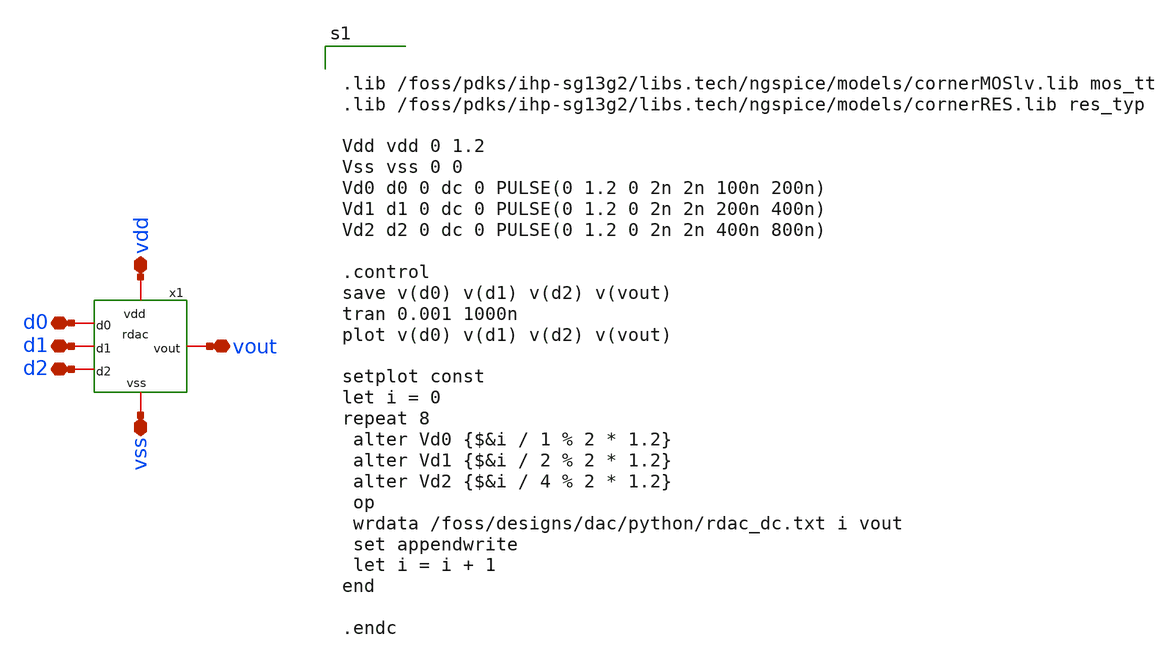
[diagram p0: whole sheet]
** sch_path: xschem/rdac_tb.sch
**.subckt rdac_tb vout vss d0 d1 d2 vdd
*.iopin vout
*.iopin vss
*.iopin d0
*.iopin d1
*.iopin d2
*.iopin vdd
x1 vdd d0 vout d1 d2 vss rdac
**** begin user architecture code


.lib /foss/pdks/ihp-sg13g2/libs.tech/ngspice/models/cornerMOSlv.lib mos_tt
.lib /foss/pdks/ihp-sg13g2/libs.tech/ngspice/models/cornerRES.lib res_typ

Vdd vdd 0 1.2
Vss vss 0 0
Vd0 d0 0 dc 0 PULSE(0 1.2 0 2n 2n 100n 200n)
Vd1 d1 0 dc 0 PULSE(0 1.2 0 2n 2n 200n 400n)
Vd2 d2 0 dc 0 PULSE(0 1.2 0 2n 2n 400n 800n)

.control
save v(d0) v(d1) v(d2) v(vout)
tran 0.001 1000n
plot v(d0) v(d1) v(d2) v(vout)

setplot const
let i = 0
repeat 8
 alter Vd0 {$&i / 1 % 2 * 1.2}
 alter Vd1 {$&i / 2 % 2 * 1.2}
 alter Vd2 {$&i / 4 % 2 * 1.2}
 op
 wrdata /foss/designs/dac/python/rdac_dc.txt i vout
 set appendwrite
 let i = i + 1
end

.endc


**** end user architecture code
**.ends

* expanding   symbol:  rdac.sym # of pins=6
** sym_path: xschem/rdac.sym
** sch_path: xschem/rdac.sch
.subckt rdac vdd d0 vout d1 d2 vss
*.iopin vout
*.iopin vdd
*.iopin d0
*.iopin vss
*.iopin d1
*.iopin d2
x1 vdd d0 net5 vss inverter
x2 vdd d1 net4 vss inverter
x3 vdd d2 net1 vss inverter
XR1 net1 vout sub! rhigh w=0.5e-6 l=10.0e-6 m=1 b=0 mm_ok=1
XR2 net4 net2 sub! rhigh w=0.5e-6 l=10.0e-6 m=1 b=0 mm_ok=1
XR3 net5 net3 sub! rhigh w=0.5e-6 l=10.0e-6 m=1 b=0 mm_ok=1
XR4 vss net3 sub! rhigh w=0.5e-6 l=10.0e-6 m=1 b=0 mm_ok=1
XR5 vout net2 sub! rhigh w=0.5e-6 l=5.0e-6 m=1 b=0 mm_ok=1
XR6 net2 net3 sub! rhigh w=0.5e-6 l=5.0e-6 m=1 b=0 mm_ok=1
.ends


* expanding   symbol:  inverter.sym # of pins=4
** sym_path: xschem/inverter.sym
** sch_path: xschem/inverter.sch
.subckt inverter vdd vin vout vss
*.iopin vout
*.iopin vss
*.iopin vin
*.iopin vdd
XM1 vout vin vss vss sg13_lv_nmos w=1.5u l=0.13u ng=1 m=1 mm_ok=1
XM2 vout vin vdd vdd sg13_lv_pmos w=3.0u l=0.13u ng=1 m=1 mm_ok=1
.ends

.end
